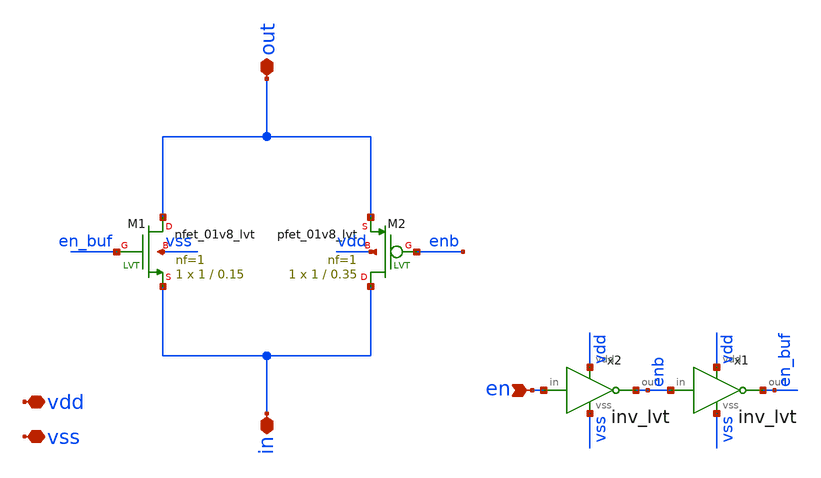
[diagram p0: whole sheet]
** sch_path: xschem/switches/passgate_min.sch
**.subckt passgate_min out en vss vdd in
*.iopin out
*.ipin en
*.iopin vss
*.iopin vdd
*.iopin in
XM1 out en_buf in vss sky130_fd_pr__nfet_01v8_lvt L=0.15 W=1 nf=1 ad='int((nf+1)/2) * W/nf * 0.29' as='int((nf+2)/2) * W/nf * 0.29'
+ pd='2*int((nf+1)/2) * (W/nf + 0.29)' ps='2*int((nf+2)/2) * (W/nf + 0.29)' nrd='0.29 / W' nrs='0.29 / W'
+ sa=0 sb=0 sd=0 mult=1 m=1
XM2 in enb out vdd sky130_fd_pr__pfet_01v8_lvt L=0.35 W=1 nf=1 ad='int((nf+1)/2) * W/nf * 0.29' as='int((nf+2)/2) * W/nf * 0.29'
+ pd='2*int((nf+1)/2) * (W/nf + 0.29)' ps='2*int((nf+2)/2) * (W/nf + 0.29)' nrd='0.29 / W' nrs='0.29 / W'
+ sa=0 sb=0 sd=0 mult=1 m=1
x2 vdd en enb vss inv_lvt
x1 vdd enb en_buf vss inv_lvt
**.ends

* expanding   symbol:  logic/inv_lvt.sym # of pins=4
** sym_path: xschem/logic/inv_lvt.sym
** sch_path: xschem/logic/inv_lvt.sch
.subckt inv_lvt vdd in out vss
*.iopin vdd
*.iopin vss
*.ipin in
*.opin out
XM1 out in vss vss sky130_fd_pr__nfet_01v8_lvt L=0.4 W=1 nf=1 ad='int((nf+1)/2) * W/nf * 0.29' as='int((nf+2)/2) * W/nf * 0.29'
+ pd='2*int((nf+1)/2) * (W/nf + 0.29)' ps='2*int((nf+2)/2) * (W/nf + 0.29)' nrd='0.29 / W' nrs='0.29 / W'
+ sa=0 sb=0 sd=0 mult=1 m=1
XM2 out in vdd vdd sky130_fd_pr__pfet_01v8_lvt L=0.4 W=1 nf=1 ad='int((nf+1)/2) * W/nf * 0.29' as='int((nf+2)/2) * W/nf * 0.29'
+ pd='2*int((nf+1)/2) * (W/nf + 0.29)' ps='2*int((nf+2)/2) * (W/nf + 0.29)' nrd='0.29 / W' nrs='0.29 / W'
+ sa=0 sb=0 sd=0 mult=1 m=1
.ends

.end
